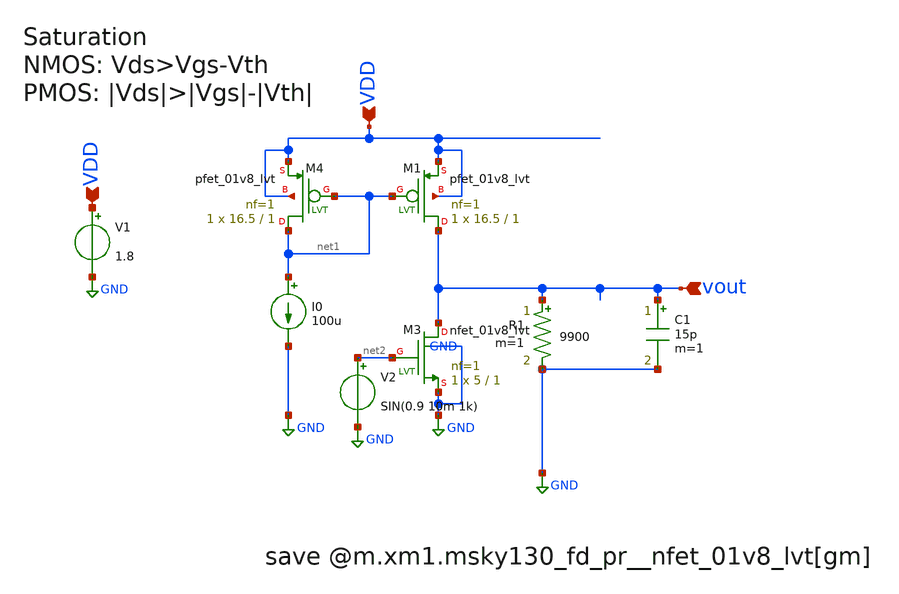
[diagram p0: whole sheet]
** sch_path: xschem/EA/commonsource (Copy).sch
**.subckt commonsource (Copy) VDD VDD vout
*.ipin VDD
*.ipin VDD
*.ipin vout
V1 VDD GND 1.8
XM1 vout net1 VDD VDD sky130_fd_pr__pfet_01v8_lvt L=1 W=16.5 nf=1 ad='int((1 + 1)/2) * 16.5 / 1 * 0.29'
+ as='int((1 + 2)/2) * 16.5 / 1 * 0.29' pd='2*int((1 + 1)/2) * (16.5 / 1 + 0.29)' ps='2*int((1 + 2)/2) * (16.5 / 1 + 0.29)'
+ nrd='0.29 / 16.5 ' nrs='0.29 / 16.5 ' sa=0 sb=0 sd=0 mult=1 m=1
I0 net1 GND 100u
XM3 vout net2 GND GND sky130_fd_pr__nfet_01v8_lvt L=1 W=5 nf=1 ad='int((1 + 1)/2) * 5 / 1 * 0.29' as='int((1 + 2)/2) * 5 / 1 * 0.29'
+ pd='2*int((1 + 1)/2) * (5 / 1 + 0.29)' ps='2*int((1 + 2)/2) * (5 / 1 + 0.29)' nrd='0.29 / 5 ' nrs='0.29 / 5 '
+ sa=0 sb=0 sd=0 mult=1 m=1
XM4 net1 net1 VDD VDD sky130_fd_pr__pfet_01v8_lvt L=1 W=16.5 nf=1 ad='int((1 + 1)/2) * 16.5 / 1 * 0.29'
+ as='int((1 + 2)/2) * 16.5 / 1 * 0.29' pd='2*int((1 + 1)/2) * (16.5 / 1 + 0.29)' ps='2*int((1 + 2)/2) * (16.5 / 1 + 0.29)'
+ nrd='0.29 / 16.5 ' nrs='0.29 / 16.5 ' sa=0 sb=0 sd=0 mult=1 m=1
V2 net2 GND SIN(0.9 10m 1k)
R1 vout GND 9900 m=1
C1 vout GND 15p m=1
**** begin user architecture code



.lib /usr/local/share/pdk/sky130A/libs.tech/ngspice/sky130.lib.spice tt
.tran 5u 3m
*.ac dec 20 1 1e12
.save all

.control
run
print @m.xm1.msky130_fd_pr__pfet_01v8_lvt[vth]
print @m.xm3.msky130_fd_pr__nfet_01v8_lvt[vth]
print @m.xm1.msky130_fd_pr__pfet_01v8_lvt[id]
print @m.xm3.msky130_fd_pr__nfet_01v8_lvt[id]
print 1/@m.xm3.msky130_fd_pr__nfet_01v8_lvt[gds]
print 1/@m.xm1.msky130_fd_pr__pfet_01v8_lvt[gds]
print @m.xm3.msky130_fd_pr__nfet_01v8_lvt[gm]
plot vout title vout
*plot db(vout/v(net2))
*plot 180*cph(vout)/pi
set wr_singlescale
set wr_vecnames
*wrdata /foss/designs/2stageCMOSOpAmp/sim_data/GainvsFreq/gain(max).txt db(vout/v(v+))
*wrdata /foss/designs/2stageCMOSOpAmp/sim_data/sample_waves/a1.3m_f1k_gain700.txt vout
*wrdata /foss/designs/2stageCMOSOpAmp/sim_data/SR/SR.txt vout

.endc


**** end user architecture code
**.ends
.GLOBAL GND
.end
